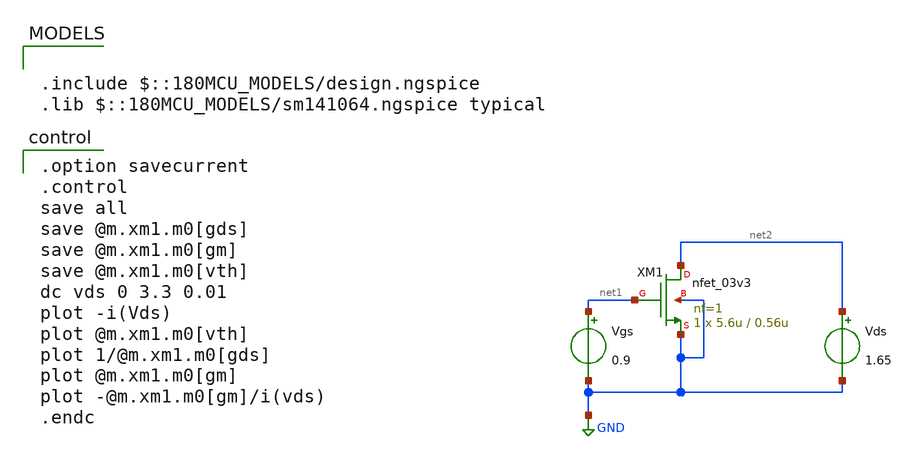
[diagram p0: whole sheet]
** sch_path: opamp/nfet_idvds_2L.sch
**.subckt nfet_idvds_2L
XM1 net2 net1 GND GND nfet_03v3 L=0.56u W=5.6u nf=1 ad='int((nf+1)/2) * W/nf * 0.18u' as='int((nf+2)/2) * W/nf * 0.18u'
+ pd='2*int((nf+1)/2) * (W/nf + 0.18u)' ps='2*int((nf+2)/2) * (W/nf + 0.18u)' nrd='0.18u / W' nrs='0.18u / W'
+ sa=0 sb=0 sd=0 m=1
Vgs net1 GND 0.9
Vds net2 GND 1.65
**** begin user architecture code

.include $::180MCU_MODELS/design.ngspice
.lib $::180MCU_MODELS/sm141064.ngspice typical


.option savecurrent
.control
save all
save @m.xm1.m0[gds]
save @m.xm1.m0[gm]
save @m.xm1.m0[vth]
dc vds 0 3.3 0.01
plot -i(Vds)
plot @m.xm1.m0[vth]
plot 1/@m.xm1.m0[gds]
plot @m.xm1.m0[gm]
plot -@m.xm1.m0[gm]/i(vds)
.endc

**** end user architecture code
**.ends
.GLOBAL GND
.end
